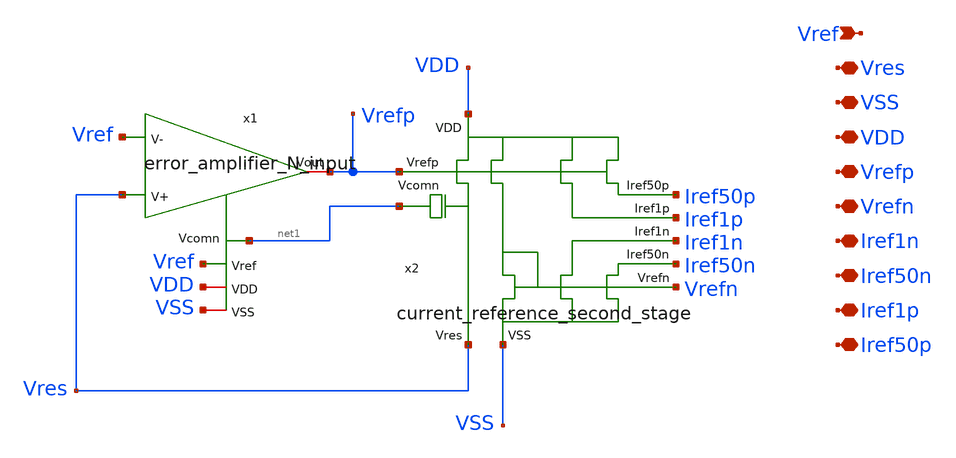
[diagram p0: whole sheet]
** sch_path: designs/current_reference_generator/xschem/current_reference_generator.sch
**.subckt current_reference_generator Vref VDD VSS Vrefp Vrefn Iref1n Iref50n Iref1p Iref50p Vres
*.ipin Vref
*.iopin VDD
*.iopin VSS
*.iopin Vrefp
*.iopin Vrefn
*.iopin Iref1n
*.iopin Iref50n
*.iopin Iref1p
*.iopin Iref50p
*.iopin Vres
x1 Vrefp Vres Vref Vref VDD VSS net1 error_amplifier_N_input
x2 net1 Vres VSS VDD Vrefp Vrefn Iref1n Iref50n Iref1p Iref50p current_reference_second_stage
**.ends
.end
